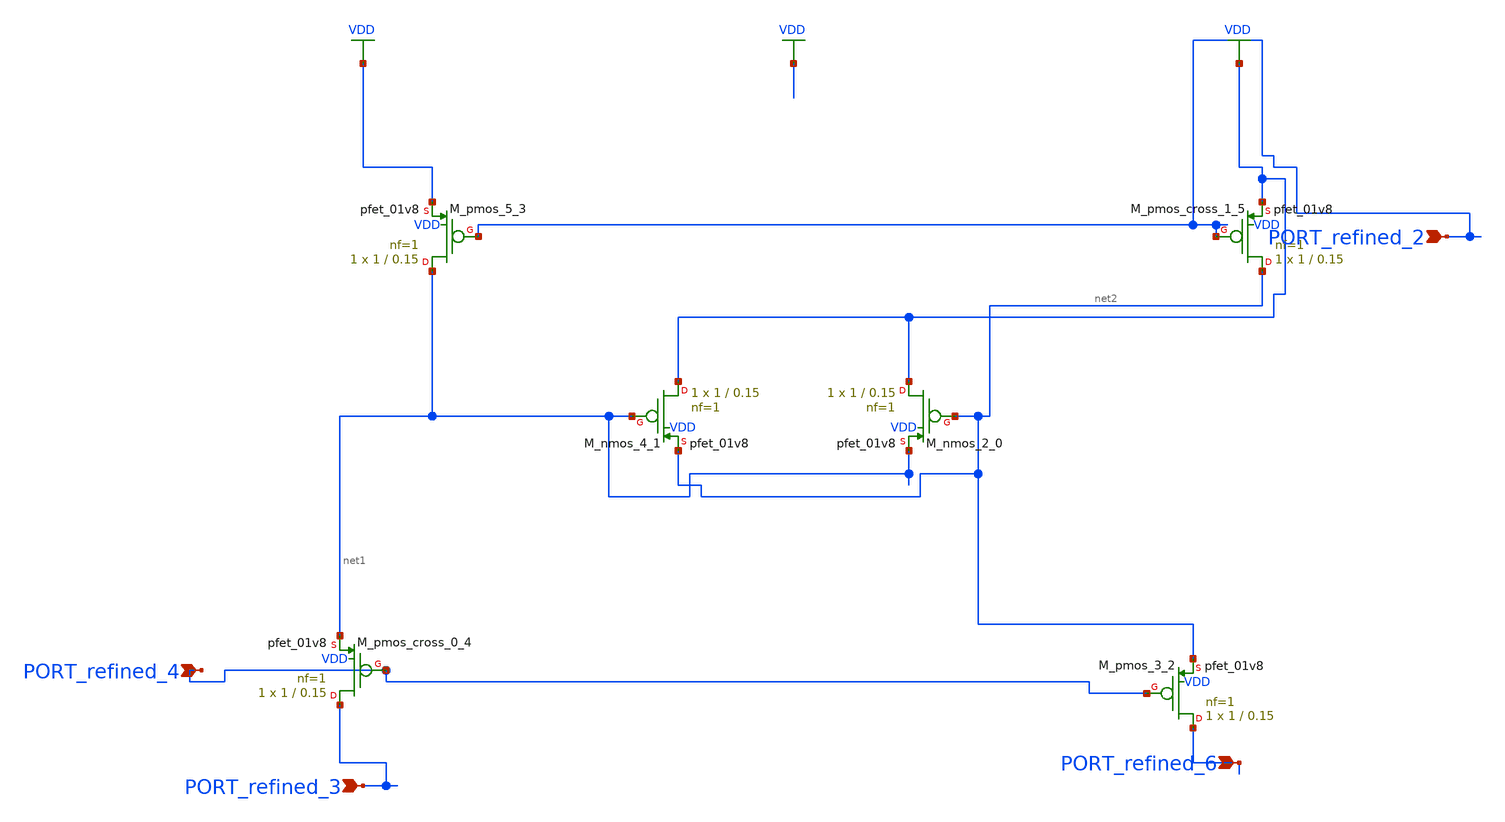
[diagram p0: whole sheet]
** sch_path: schematics/AMSNet/697.sch
**.subckt 697 PORT_refined_3 PORT_refined_2 PORT_refined_4 PORT_refined_6
*.ipin PORT_refined_3
*.ipin PORT_refined_2
*.ipin PORT_refined_4
*.ipin PORT_refined_6
XM_nmos_2_0 VDD net2 net1 VDD sky130_fd_pr__pfet_01v8 L=0.15 W=1 nf=1 ad='int((1 + 1)/2) * 1 / 1 * 0.29'
+ as='int((1 + 2)/2) * 1 / 1 * 0.29' pd='2*int((1 + 1)/2) * (1 / 1 + 0.29)' ps='2*int((1 + 2)/2) * (1 / 1 + 0.29)'
+ nrd='0.29 / 1 ' nrs='0.29 / 1 ' sa=0 sb=0 sd=0 mult=1 m=1
XM_nmos_4_1 VDD net1 net2 VDD sky130_fd_pr__pfet_01v8 L=0.15 W=1 nf=1 ad='int((1 + 1)/2) * 1 / 1 * 0.29'
+ as='int((1 + 2)/2) * 1 / 1 * 0.29' pd='2*int((1 + 1)/2) * (1 / 1 + 0.29)' ps='2*int((1 + 2)/2) * (1 / 1 + 0.29)'
+ nrd='0.29 / 1 ' nrs='0.29 / 1 ' sa=0 sb=0 sd=0 mult=1 m=1
XM_pmos_3_2 PORT_refined_6 PORT_refined_4 net2 VDD sky130_fd_pr__pfet_01v8 L=0.15 W=1 nf=1 ad='int((1 + 1)/2) * 1 / 1 * 0.29'
+ as='int((1 + 2)/2) * 1 / 1 * 0.29' pd='2*int((1 + 1)/2) * (1 / 1 + 0.29)' ps='2*int((1 + 2)/2) * (1 / 1 + 0.29)'
+ nrd='0.29 / 1 ' nrs='0.29 / 1 ' sa=0 sb=0 sd=0 mult=1 m=1
XM_pmos_5_3 net1 PORT_refined_2 VDD VDD sky130_fd_pr__pfet_01v8 L=0.15 W=1 nf=1 ad='int((1 + 1)/2) * 1 / 1 * 0.29'
+ as='int((1 + 2)/2) * 1 / 1 * 0.29' pd='2*int((1 + 1)/2) * (1 / 1 + 0.29)' ps='2*int((1 + 2)/2) * (1 / 1 + 0.29)'
+ nrd='0.29 / 1 ' nrs='0.29 / 1 ' sa=0 sb=0 sd=0 mult=1 m=1
XM_pmos_cross_0_4 PORT_refined_3 PORT_refined_4 net1 VDD sky130_fd_pr__pfet_01v8 L=0.15 W=1 nf=1 ad='int((1 + 1)/2) * 1 / 1 * 0.29'
+ as='int((1 + 2)/2) * 1 / 1 * 0.29' pd='2*int((1 + 1)/2) * (1 / 1 + 0.29)' ps='2*int((1 + 2)/2) * (1 / 1 + 0.29)'
+ nrd='0.29 / 1 ' nrs='0.29 / 1 ' sa=0 sb=0 sd=0 mult=1 m=1
XM_pmos_cross_1_5 net2 PORT_refined_2 VDD VDD sky130_fd_pr__pfet_01v8 L=0.15 W=1 nf=1 ad='int((1 + 1)/2) * 1 / 1 * 0.29'
+ as='int((1 + 2)/2) * 1 / 1 * 0.29' pd='2*int((1 + 1)/2) * (1 / 1 + 0.29)' ps='2*int((1 + 2)/2) * (1 / 1 + 0.29)'
+ nrd='0.29 / 1 ' nrs='0.29 / 1 ' sa=0 sb=0 sd=0 mult=1 m=1
**.ends
.GLOBAL VDD
.end
